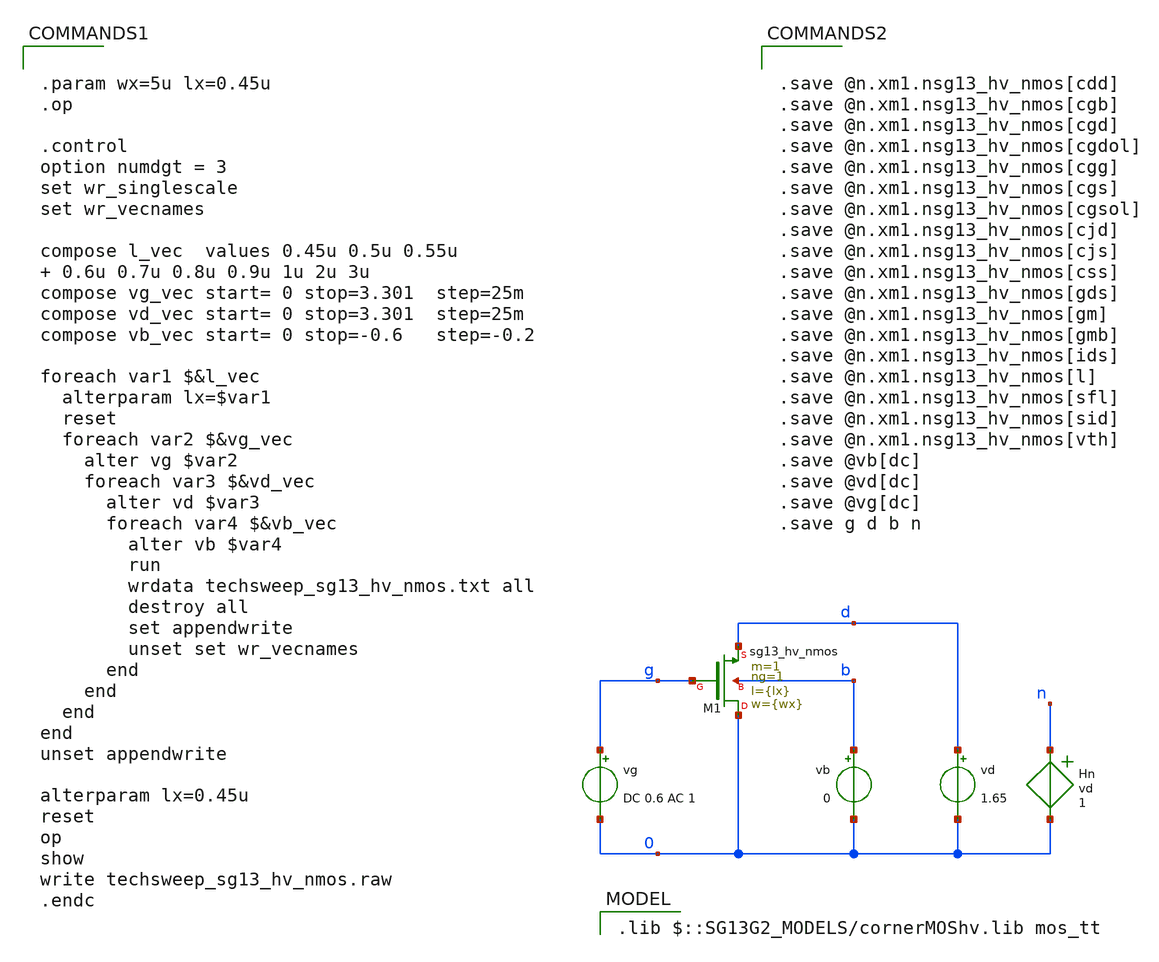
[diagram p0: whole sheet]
** sch_path: model/calculations/ihp-sg13g2_lookup/techsweep_sg13_hv_nmos.sch
**.subckt techsweep_sg13_hv_nmos
vg g 0 DC 0.6 AC 1
vd d 0 1.65
vb b 0 0
Hn n 0 vd 1
XM1 0 g d b sg13_hv_nmos w={wx} l={lx} ng=1 m=1 mm_ok=1
**** begin user architecture code


.param wx=5u lx=0.45u
.op

.control
option numdgt = 3
set wr_singlescale
set wr_vecnames

compose l_vec  values 0.45u 0.5u 0.55u  0.6u 0.7u 0.8u 0.9u 1u 2u 3u
compose vg_vec start= 0 stop=3.301  step=25m
compose vd_vec start= 0 stop=3.301  step=25m
compose vb_vec start= 0 stop=-0.6   step=-0.2

foreach var1 $&l_vec
  alterparam lx=$var1
  reset
  foreach var2 $&vg_vec
    alter vg $var2
    foreach var3 $&vd_vec
      alter vd $var3
      foreach var4 $&vb_vec
        alter vb $var4
        run
        wrdata techsweep_sg13_hv_nmos.txt all
        destroy all
        set appendwrite
        unset set wr_vecnames
      end
    end
  end
end
unset appendwrite

alterparam lx=0.45u
reset
op
show
write techsweep_sg13_hv_nmos.raw
.endc




.save @n.xm1.nsg13_hv_nmos[cdd]
.save @n.xm1.nsg13_hv_nmos[cgb]
.save @n.xm1.nsg13_hv_nmos[cgd]
.save @n.xm1.nsg13_hv_nmos[cgdol]
.save @n.xm1.nsg13_hv_nmos[cgg]
.save @n.xm1.nsg13_hv_nmos[cgs]
.save @n.xm1.nsg13_hv_nmos[cgsol]
.save @n.xm1.nsg13_hv_nmos[cjd]
.save @n.xm1.nsg13_hv_nmos[cjs]
.save @n.xm1.nsg13_hv_nmos[css]
.save @n.xm1.nsg13_hv_nmos[gds]
.save @n.xm1.nsg13_hv_nmos[gm]
.save @n.xm1.nsg13_hv_nmos[gmb]
.save @n.xm1.nsg13_hv_nmos[ids]
.save @n.xm1.nsg13_hv_nmos[l]
.save @n.xm1.nsg13_hv_nmos[sfl]
.save @n.xm1.nsg13_hv_nmos[sid]
.save @n.xm1.nsg13_hv_nmos[vth]
.save @vb[dc]
.save @vd[dc]
.save @vg[dc]
.save g d b n


 .lib $::SG13G2_MODELS/cornerMOShv.lib mos_tt
**** end user architecture code
**.ends
.end
